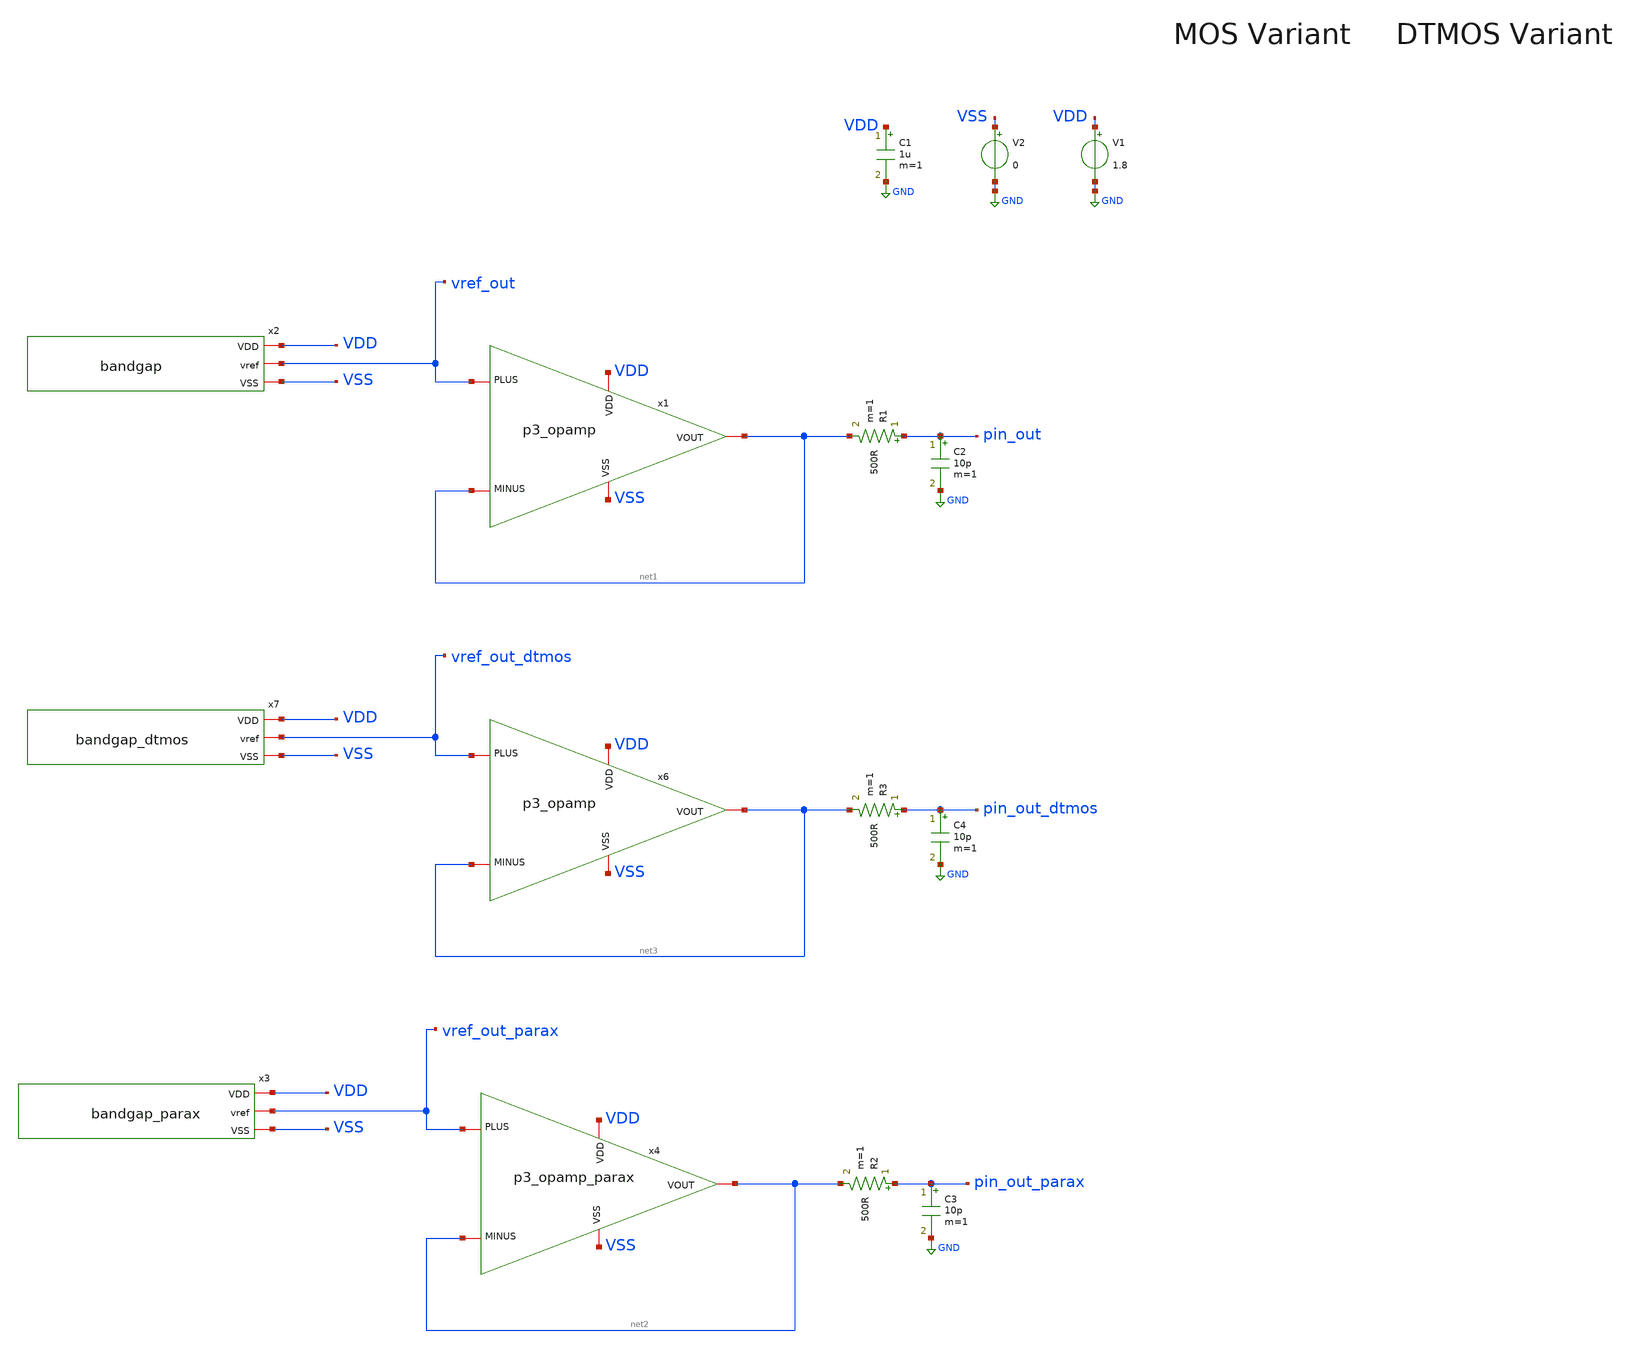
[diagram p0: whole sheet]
** sch_path: xschem/tb_bandgap.sch
**.subckt tb_bandgap
x2 VDD vref_out VSS bandgap
V1 VDD GND 1.8
V2 VSS GND 0
C1 VDD GND 1u m=1
x1 VDD net1 vref_out net1 VSS p3_opamp
R1 pin_out net1 500R m=1
C2 pin_out GND 10p m=1
x3 VDD vref_out_parax VSS bandgap_parax
x4 VDD net2 vref_out_parax net2 VSS p3_opamp_parax
R2 pin_out_parax net2 500R m=1
C3 pin_out_parax GND 10p m=1
x6 VDD net3 vref_out_dtmos net3 VSS p3_opamp
R3 pin_out_dtmos net3 500R m=1
C4 pin_out_dtmos GND 10p m=1
x7 VDD vref_out_dtmos VSS bandgap_dtmos
**** begin user architecture code

** opencircuitdesign pdks install
.lib $::SKYWATER_MODELS/sky130.lib.spice tt






.control

 dc v1 1.3 2 0.01
 write tb_bandgap.raw
 set appendwrite

 reset
 dc temp 10 100 1
 write tb_bandgap.raw

.endc



**** end user architecture code
**.ends
.GLOBAL GND
.end
